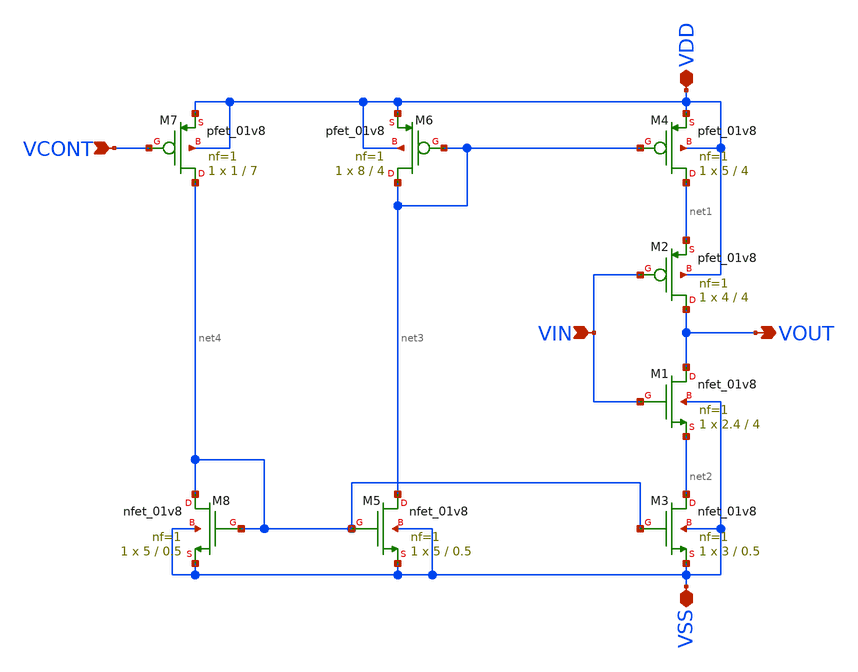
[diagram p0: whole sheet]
** sch_path: xschem/stage_v5p1.sch
**.subckt stage_v5p1 VIN VOUT VDD VSS VCONT
*.ipin VIN
*.opin VOUT
*.iopin VDD
*.iopin VSS
*.ipin VCONT
XM1 VOUT VIN net2 VSS sky130_fd_pr__nfet_01v8 L=4 W=2.4 nf=1 ad='int((nf+1)/2) * W/nf * 0.29' as='int((nf+2)/2) * W/nf * 0.29'
+ pd='2*int((nf+1)/2) * (W/nf + 0.29)' ps='2*int((nf+2)/2) * (W/nf + 0.29)' nrd='0.29 / W' nrs='0.29 / W'
+ sa=0 sb=0 sd=0 mult=1 m=1
XM2 VOUT VIN net1 VDD sky130_fd_pr__pfet_01v8 L=4 W=4 nf=1 ad='int((nf+1)/2) * W/nf * 0.29' as='int((nf+2)/2) * W/nf * 0.29'
+ pd='2*int((nf+1)/2) * (W/nf + 0.29)' ps='2*int((nf+2)/2) * (W/nf + 0.29)' nrd='0.29 / W' nrs='0.29 / W'
+ sa=0 sb=0 sd=0 mult=1 m=1
XM3 net2 net4 VSS VSS sky130_fd_pr__nfet_01v8 L=0.5 W=3 nf=1 ad='int((nf+1)/2) * W/nf * 0.29' as='int((nf+2)/2) * W/nf * 0.29'
+ pd='2*int((nf+1)/2) * (W/nf + 0.29)' ps='2*int((nf+2)/2) * (W/nf + 0.29)' nrd='0.29 / W' nrs='0.29 / W'
+ sa=0 sb=0 sd=0 mult=1 m=1
XM4 net1 net3 VDD VDD sky130_fd_pr__pfet_01v8 L=4 W=5 nf=1 ad='int((nf+1)/2) * W/nf * 0.29' as='int((nf+2)/2) * W/nf * 0.29'
+ pd='2*int((nf+1)/2) * (W/nf + 0.29)' ps='2*int((nf+2)/2) * (W/nf + 0.29)' nrd='0.29 / W' nrs='0.29 / W'
+ sa=0 sb=0 sd=0 mult=1 m=1
XM5 net3 net4 VSS VSS sky130_fd_pr__nfet_01v8 L=0.5 W=5 nf=1 ad='int((nf+1)/2) * W/nf * 0.29' as='int((nf+2)/2) * W/nf * 0.29'
+ pd='2*int((nf+1)/2) * (W/nf + 0.29)' ps='2*int((nf+2)/2) * (W/nf + 0.29)' nrd='0.29 / W' nrs='0.29 / W'
+ sa=0 sb=0 sd=0 mult=1 m=1
XM6 net3 net3 VDD VDD sky130_fd_pr__pfet_01v8 L=4 W=8 nf=1 ad='int((nf+1)/2) * W/nf * 0.29' as='int((nf+2)/2) * W/nf * 0.29'
+ pd='2*int((nf+1)/2) * (W/nf + 0.29)' ps='2*int((nf+2)/2) * (W/nf + 0.29)' nrd='0.29 / W' nrs='0.29 / W'
+ sa=0 sb=0 sd=0 mult=1 m=1
XM7 net4 VCONT VDD VDD sky130_fd_pr__pfet_01v8 L=7 W=1 nf=1 ad='int((nf+1)/2) * W/nf * 0.29' as='int((nf+2)/2) * W/nf * 0.29'
+ pd='2*int((nf+1)/2) * (W/nf + 0.29)' ps='2*int((nf+2)/2) * (W/nf + 0.29)' nrd='0.29 / W' nrs='0.29 / W'
+ sa=0 sb=0 sd=0 mult=1 m=1
XM8 net4 net4 VSS VSS sky130_fd_pr__nfet_01v8 L=0.5 W=5 nf=1 ad='int((nf+1)/2) * W/nf * 0.29' as='int((nf+2)/2) * W/nf * 0.29'
+ pd='2*int((nf+1)/2) * (W/nf + 0.29)' ps='2*int((nf+2)/2) * (W/nf + 0.29)' nrd='0.29 / W' nrs='0.29 / W'
+ sa=0 sb=0 sd=0 mult=1 m=1
**.ends
.end
